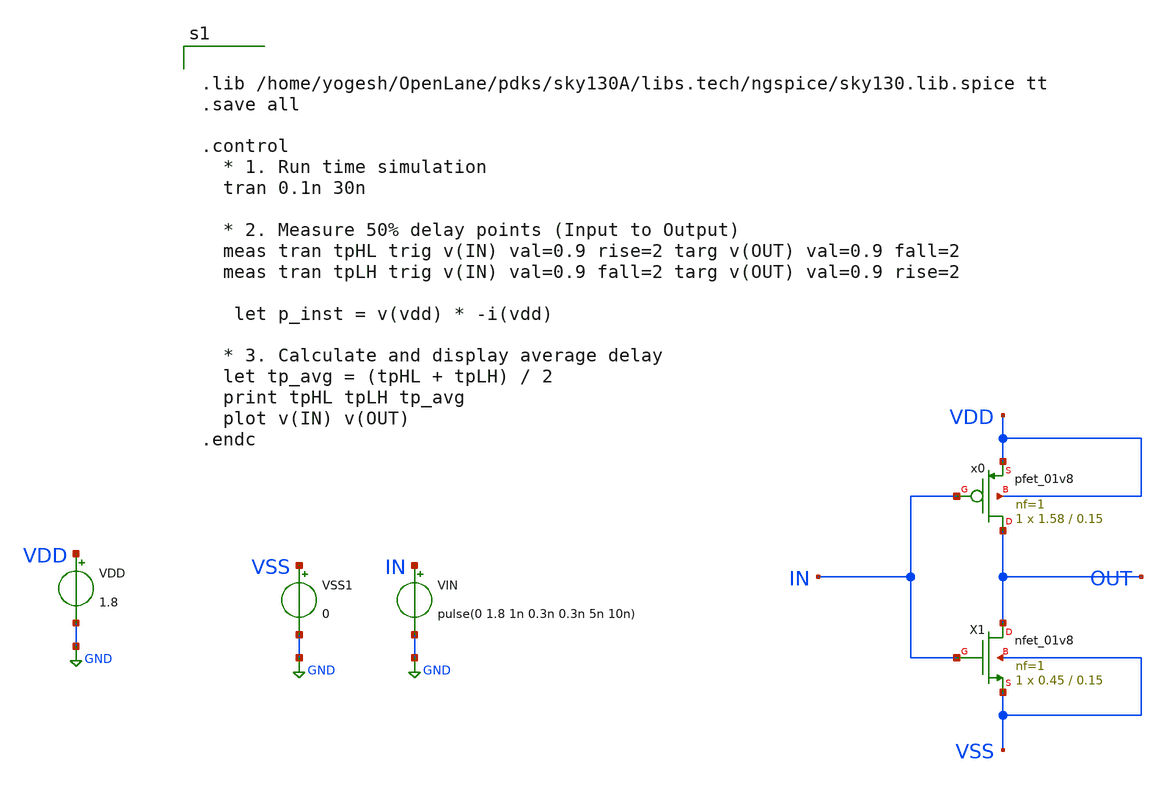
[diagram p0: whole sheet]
** sch_path: OneDrive/Documents/CMOS-Inverter-Design-and-Analysis-using-Sky130pdk-main/xschem/cmos_invF.sch
**.subckt cmos_invF
XX1 OUT IN VSS VSS sky130_fd_pr__nfet_01v8 L=0.15 W=0.45 nf=1 ad='int((nf+1)/2) * W/nf * 0.29' as='int((nf+2)/2) * W/nf * 0.29'
+ pd='2*int((nf+1)/2) * (W/nf + 0.29)' ps='2*int((nf+2)/2) * (W/nf + 0.29)' nrd='0.29 / W' nrs='0.29 / W'
+ sa=0 sb=0 sd=0 mult=1 m=1
VIN IN GND pulse(0 1.8 1n 0.3n 0.3n 5n 10n)
VSS1 VSS GND 0
VDD VDD GND 1.8
Xx0 OUT IN VDD VDD sky130_fd_pr__pfet_01v8 L=0.15 W=1.58 nf=1 ad='int((nf+1)/2) * W/nf * 0.29' as='int((nf+2)/2) * W/nf * 0.29'
+ pd='2*int((nf+1)/2) * (W/nf + 0.29)' ps='2*int((nf+2)/2) * (W/nf + 0.29)' nrd='0.29 / W' nrs='0.29 / W'
+ sa=0 sb=0 sd=0 mult=1 m=1
**** begin user architecture code


.lib /home/yogesh/OpenLane/pdks/sky130A/libs.tech/ngspice/sky130.lib.spice tt
.save all

.control
  * 1. Run time simulation
  tran 0.1n 30n

  * 2. Measure 50% delay points (Input to Output)
  meas tran tpHL trig v(IN) val=0.9 rise=2 targ v(OUT) val=0.9 fall=2
  meas tran tpLH trig v(IN) val=0.9 fall=2 targ v(OUT) val=0.9 rise=2

   let p_inst = v(vdd) * -i(vdd)

  * 3. Calculate and display average delay
  let tp_avg = (tpHL + tpLH) / 2
  print tpHL tpLH tp_avg
  plot v(IN) v(OUT)
.endc

**** end user architecture code
**.ends
.GLOBAL GND
.end
